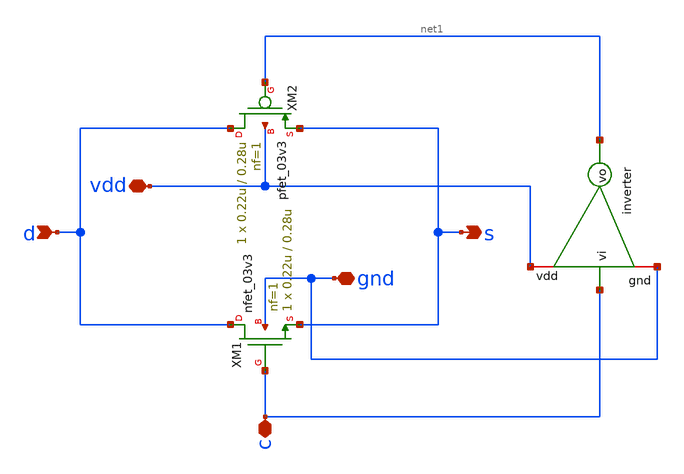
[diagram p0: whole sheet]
** sch_path: src/schematic/TG/transgate.sch
**.subckt transgate gnd vdd c d s
*.iopin gnd
*.iopin vdd
*.iopin c
*.ipin d
*.opin s
XM1 d c s gnd nfet_03v3 L=0.28u W=0.22u nf=1 ad='int((nf+1)/2) * W/nf * 0.18u' as='int((nf+2)/2) * W/nf * 0.18u'
+ pd='2*int((nf+1)/2) * (W/nf + 0.18u)' ps='2*int((nf+2)/2) * (W/nf + 0.18u)' nrd='0.18u / W' nrs='0.18u / W'
+ sa=0 sb=0 sd=0 m=1
XM2 d net1 s vdd pfet_03v3 L=0.28u W=0.22u nf=1 ad='int((nf+1)/2) * W/nf * 0.18u' as='int((nf+2)/2) * W/nf * 0.18u'
+ pd='2*int((nf+1)/2) * (W/nf + 0.18u)' ps='2*int((nf+2)/2) * (W/nf + 0.18u)' nrd='0.18u / W' nrs='0.18u / W'
+ sa=0 sb=0 sd=0 m=1
x1 vdd c net1 gnd inverter
**.ends

* expanding   symbol:  src/schematic/INV/inverter.sym # of pins=4
** sym_path: src/schematic/TG/inverter.sym
** sch_path: src/schematic/TG/inverter.sch
.subckt inverter vdd vi vo gnd
*.ipin vi
*.opin vo
*.iopin vdd
*.iopin gnd
XM1 vo vi vdd vdd pfet_03v3 L=0.28u W=0.22u nf=1 ad='int((nf+1)/2) * W/nf * 0.18u' as='int((nf+2)/2) * W/nf * 0.18u'
+ pd='2*int((nf+1)/2) * (W/nf + 0.18u)' ps='2*int((nf+2)/2) * (W/nf + 0.18u)' nrd='0.18u / W' nrs='0.18u / W'
+ sa=0 sb=0 sd=0 m=1
XM2 vo vi gnd gnd nfet_03v3 L=0.28u W=0.22u nf=1 ad='int((nf+1)/2) * W/nf * 0.18u' as='int((nf+2)/2) * W/nf * 0.18u'
+ pd='2*int((nf+1)/2) * (W/nf + 0.18u)' ps='2*int((nf+2)/2) * (W/nf + 0.18u)' nrd='0.18u / W' nrs='0.18u / W'
+ sa=0 sb=0 sd=0 m=1
.ends

.end
